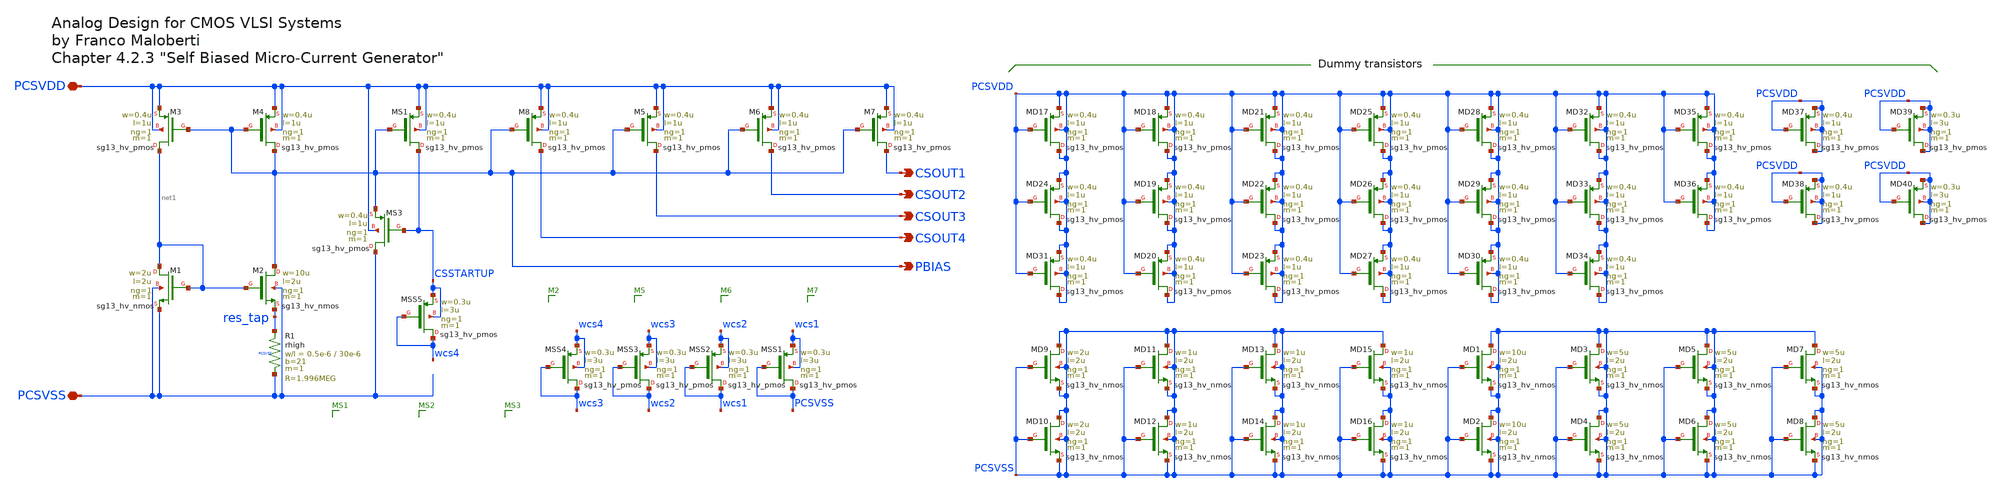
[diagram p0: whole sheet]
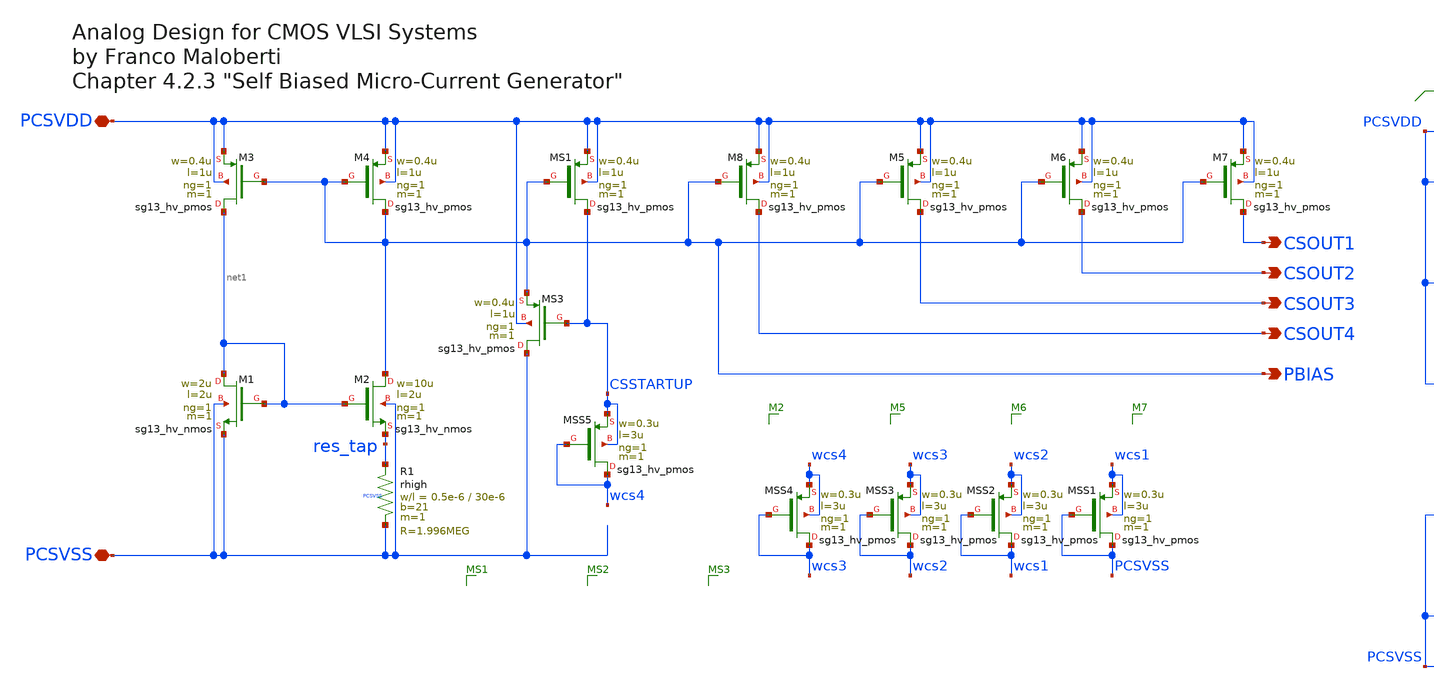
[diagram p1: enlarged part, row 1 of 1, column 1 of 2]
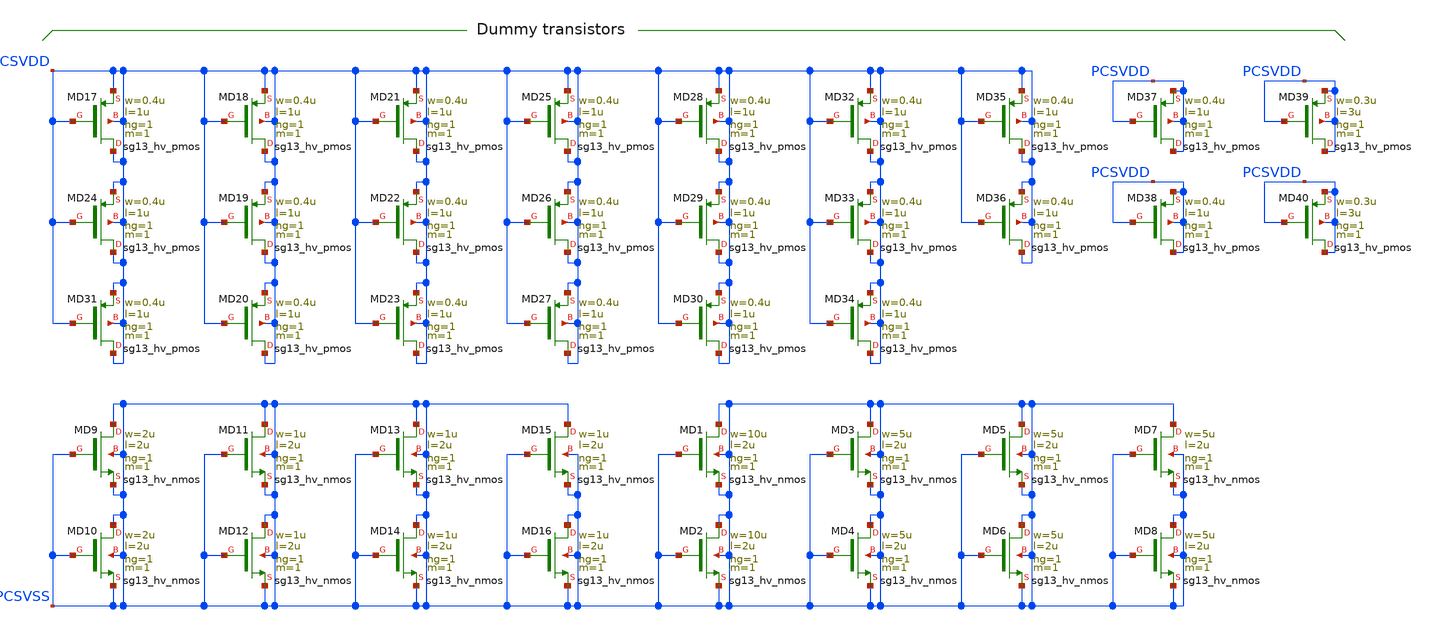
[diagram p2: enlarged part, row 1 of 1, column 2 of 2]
** sch_path: macros/heichips26_FAIf/macros/ptat_current_source/schematic/xschem/ptat_curr_gen.sch
**.subckt ptat_curr_gen PCSVDD PCSVSS CSOUT1 CSOUT2 CSOUT3 PBIAS CSOUT4
*.iopin PCSVDD
*.iopin PCSVSS
*.opin CSOUT1
*.opin CSOUT2
*.opin CSOUT3
*.opin PBIAS
*.opin CSOUT4
XM1 net1 net1 PCSVSS PCSVSS sg13_hv_nmos w=2u l=2u ng=1 m=1 mm_ok=1
XM2 PBIAS net1 res_tap PCSVSS sg13_hv_nmos w=10u l=2u ng=1 m=1 mm_ok=1
XM3 net1 PBIAS PCSVDD PCSVDD sg13_hv_pmos w=0.4u l=1u ng=1 m=1 mm_ok=1
XM4 PBIAS PBIAS PCSVDD PCSVDD sg13_hv_pmos w=0.4u l=1u ng=1 m=1 mm_ok=1
XR1 res_tap PCSVSS PCSVSS rhigh w=0.5e-6 l=30e-6 m=1 b=21 mm_ok=1
XM5 CSOUT3 PBIAS PCSVDD PCSVDD sg13_hv_pmos w=0.4u l=1u ng=1 m=1 mm_ok=1
XM6 CSOUT2 PBIAS PCSVDD PCSVDD sg13_hv_pmos w=0.4u l=1u ng=1 m=1 mm_ok=1
XM7 CSOUT1 PBIAS PCSVDD PCSVDD sg13_hv_pmos w=0.4u l=1u ng=1 m=1 mm_ok=1
XMD1 PCSVSS PCSVSS PCSVSS PCSVSS sg13_hv_nmos w=10u l=2u ng=1 m=1 mm_ok=1
XMD2 PCSVSS PCSVSS PCSVSS PCSVSS sg13_hv_nmos w=10u l=2u ng=1 m=1 mm_ok=1
XMD3 PCSVSS PCSVSS PCSVSS PCSVSS sg13_hv_nmos w=5u l=2u ng=1 m=1 mm_ok=1
XMD4 PCSVSS PCSVSS PCSVSS PCSVSS sg13_hv_nmos w=5u l=2u ng=1 m=1 mm_ok=1
XMD5 PCSVSS PCSVSS PCSVSS PCSVSS sg13_hv_nmos w=5u l=2u ng=1 m=1 mm_ok=1
XMD6 PCSVSS PCSVSS PCSVSS PCSVSS sg13_hv_nmos w=5u l=2u ng=1 m=1 mm_ok=1
XMD7 PCSVSS PCSVSS PCSVSS PCSVSS sg13_hv_nmos w=5u l=2u ng=1 m=1 mm_ok=1
XMD8 PCSVSS PCSVSS PCSVSS PCSVSS sg13_hv_nmos w=5u l=2u ng=1 m=1 mm_ok=1
XMD9 PCSVSS PCSVSS PCSVSS PCSVSS sg13_hv_nmos w=2u l=2u ng=1 m=1 mm_ok=1
XMD10 PCSVSS PCSVSS PCSVSS PCSVSS sg13_hv_nmos w=2u l=2u ng=1 m=1 mm_ok=1
XMD11 PCSVSS PCSVSS PCSVSS PCSVSS sg13_hv_nmos w=1u l=2u ng=1 m=1 mm_ok=1
XMD12 PCSVSS PCSVSS PCSVSS PCSVSS sg13_hv_nmos w=1u l=2u ng=1 m=1 mm_ok=1
XMD13 PCSVSS PCSVSS PCSVSS PCSVSS sg13_hv_nmos w=1u l=2u ng=1 m=1 mm_ok=1
XMD14 PCSVSS PCSVSS PCSVSS PCSVSS sg13_hv_nmos w=1u l=2u ng=1 m=1 mm_ok=1
XMD15 PCSVSS PCSVSS PCSVSS PCSVSS sg13_hv_nmos w=1u l=2u ng=1 m=1 mm_ok=1
XMD16 PCSVSS PCSVSS PCSVSS PCSVSS sg13_hv_nmos w=1u l=2u ng=1 m=1 mm_ok=1
XMD17 PCSVDD PCSVDD PCSVDD PCSVDD sg13_hv_pmos w=0.4u l=1u ng=1 m=1 mm_ok=1
XMD24 PCSVDD PCSVDD PCSVDD PCSVDD sg13_hv_pmos w=0.4u l=1u ng=1 m=1 mm_ok=1
XMD31 PCSVDD PCSVDD PCSVDD PCSVDD sg13_hv_pmos w=0.4u l=1u ng=1 m=1 mm_ok=1
XMD18 PCSVDD PCSVDD PCSVDD PCSVDD sg13_hv_pmos w=0.4u l=1u ng=1 m=1 mm_ok=1
XMD19 PCSVDD PCSVDD PCSVDD PCSVDD sg13_hv_pmos w=0.4u l=1u ng=1 m=1 mm_ok=1
XMD20 PCSVDD PCSVDD PCSVDD PCSVDD sg13_hv_pmos w=0.4u l=1u ng=1 m=1 mm_ok=1
XMD21 PCSVDD PCSVDD PCSVDD PCSVDD sg13_hv_pmos w=0.4u l=1u ng=1 m=1 mm_ok=1
XMD22 PCSVDD PCSVDD PCSVDD PCSVDD sg13_hv_pmos w=0.4u l=1u ng=1 m=1 mm_ok=1
XMD23 PCSVDD PCSVDD PCSVDD PCSVDD sg13_hv_pmos w=0.4u l=1u ng=1 m=1 mm_ok=1
XMD25 PCSVDD PCSVDD PCSVDD PCSVDD sg13_hv_pmos w=0.4u l=1u ng=1 m=1 mm_ok=1
XMD26 PCSVDD PCSVDD PCSVDD PCSVDD sg13_hv_pmos w=0.4u l=1u ng=1 m=1 mm_ok=1
XMD27 PCSVDD PCSVDD PCSVDD PCSVDD sg13_hv_pmos w=0.4u l=1u ng=1 m=1 mm_ok=1
XMD28 PCSVDD PCSVDD PCSVDD PCSVDD sg13_hv_pmos w=0.4u l=1u ng=1 m=1 mm_ok=1
XMD29 PCSVDD PCSVDD PCSVDD PCSVDD sg13_hv_pmos w=0.4u l=1u ng=1 m=1 mm_ok=1
XMD30 PCSVDD PCSVDD PCSVDD PCSVDD sg13_hv_pmos w=0.4u l=1u ng=1 m=1 mm_ok=1
XMD32 PCSVDD PCSVDD PCSVDD PCSVDD sg13_hv_pmos w=0.4u l=1u ng=1 m=1 mm_ok=1
XMD33 PCSVDD PCSVDD PCSVDD PCSVDD sg13_hv_pmos w=0.4u l=1u ng=1 m=1 mm_ok=1
XMD34 PCSVDD PCSVDD PCSVDD PCSVDD sg13_hv_pmos w=0.4u l=1u ng=1 m=1 mm_ok=1
XMD35 PCSVDD PCSVDD PCSVDD PCSVDD sg13_hv_pmos w=0.4u l=1u ng=1 m=1 mm_ok=1
XMD36 PCSVDD PCSVDD PCSVDD PCSVDD sg13_hv_pmos w=0.4u l=1u ng=1 m=1 mm_ok=1
XMS1 CSSTARTUP PBIAS PCSVDD PCSVDD sg13_hv_pmos w=0.4u l=1u ng=1 m=1 mm_ok=1
XMS3 PCSVSS CSSTARTUP PBIAS PCSVDD sg13_hv_pmos w=0.4u l=1u ng=1 m=1 mm_ok=1
XMSS5 wcs4 wcs4 CSSTARTUP CSSTARTUP sg13_hv_pmos w=0.3u l=3u ng=1 m=1 mm_ok=1
XM8 CSOUT4 PBIAS PCSVDD PCSVDD sg13_hv_pmos w=0.4u l=1u ng=1 m=1 mm_ok=1
XMSS4 wcs3 wcs3 wcs4 wcs4 sg13_hv_pmos w=0.3u l=3u ng=1 m=1 mm_ok=1
XMSS3 wcs2 wcs2 wcs3 wcs3 sg13_hv_pmos w=0.3u l=3u ng=1 m=1 mm_ok=1
XMSS2 wcs1 wcs1 wcs2 wcs2 sg13_hv_pmos w=0.3u l=3u ng=1 m=1 mm_ok=1
XMSS1 PCSVSS PCSVSS wcs1 wcs1 sg13_hv_pmos w=0.3u l=3u ng=1 m=1 mm_ok=1
XMD37 PCSVDD PCSVDD PCSVDD PCSVDD sg13_hv_pmos w=0.4u l=1u ng=1 m=1 mm_ok=1
XMD38 PCSVDD PCSVDD PCSVDD PCSVDD sg13_hv_pmos w=0.4u l=1u ng=1 m=1 mm_ok=1
XMD39 PCSVDD PCSVDD PCSVDD PCSVDD sg13_hv_pmos w=0.3u l=3u ng=1 m=1 mm_ok=1
XMD40 PCSVDD PCSVDD PCSVDD PCSVDD sg13_hv_pmos w=0.3u l=3u ng=1 m=1 mm_ok=1
**.ends
.end
